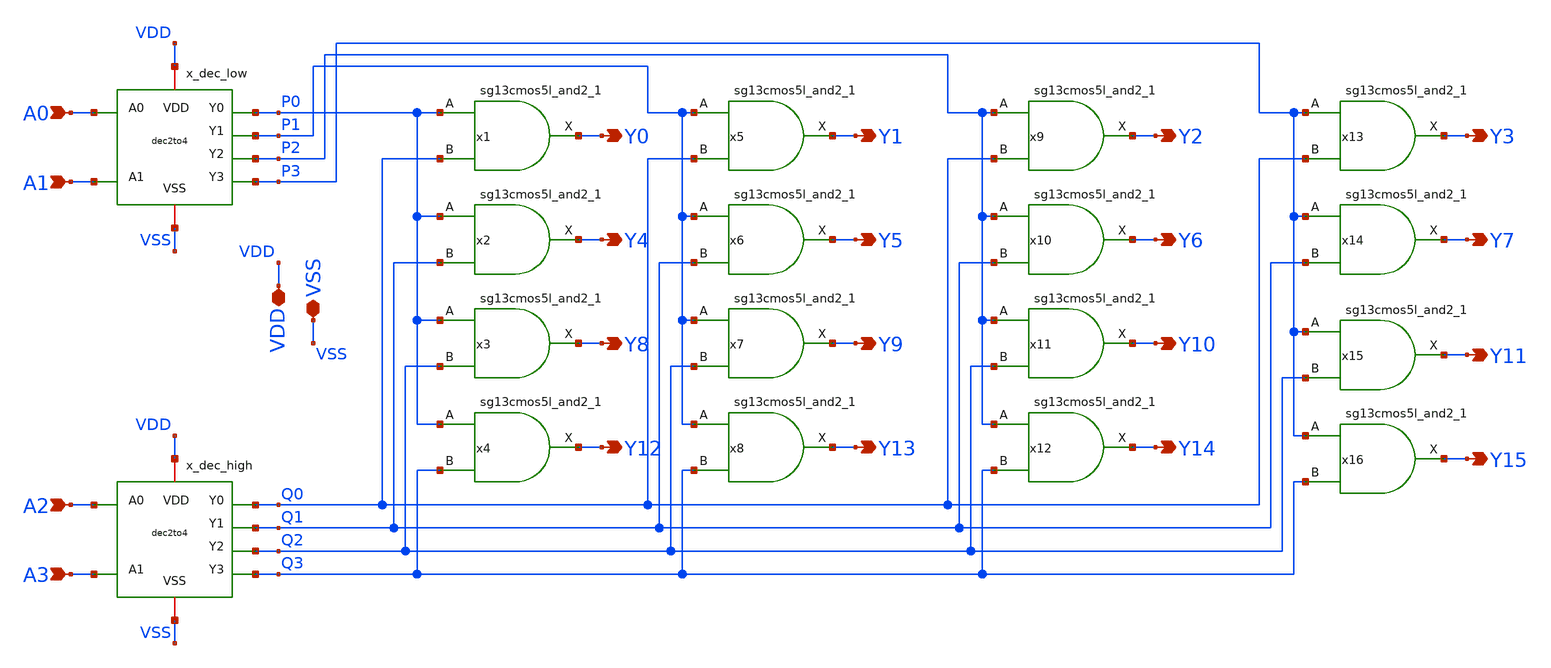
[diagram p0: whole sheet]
** sch_path: designs/libs/core_digital/dec4to16/dec4to16.sch
**.subckt dec4to16 A0 A1 A2 A3 VDD VSS Y0 Y1 Y2 Y3 Y4 Y5 Y6 Y7 Y8 Y9 Y10 Y11 Y12 Y13 Y14 Y15
*.ipin A0
*.ipin A1
*.ipin A2
*.ipin A3
*.iopin VDD
*.iopin VSS
*.opin Y0
*.opin Y1
*.opin Y2
*.opin Y3
*.opin Y4
*.opin Y5
*.opin Y6
*.opin Y7
*.opin Y8
*.opin Y9
*.opin Y10
*.opin Y11
*.opin Y12
*.opin Y13
*.opin Y14
*.opin Y15
x_dec_low A0 A1 P0 P1 P2 P3 VDD VSS dec2to4
x_dec_high A2 A3 Q0 Q1 Q2 Q3 VDD VSS dec2to4
x1 Y0 P0 Q0 VDD VSS sg13cmos5l_and2_1
x2 Y4 P0 Q1 VDD VSS sg13cmos5l_and2_1
x3 Y8 P0 Q2 VDD VSS sg13cmos5l_and2_1
x4 Y12 P0 Q3 VDD VSS sg13cmos5l_and2_1
x5 Y1 P1 Q0 VDD VSS sg13cmos5l_and2_1
x6 Y5 P1 Q1 VDD VSS sg13cmos5l_and2_1
x7 Y9 P1 Q2 VDD VSS sg13cmos5l_and2_1
x8 Y13 P1 Q3 VDD VSS sg13cmos5l_and2_1
x9 Y2 P2 Q0 VDD VSS sg13cmos5l_and2_1
x10 Y6 P2 Q1 VDD VSS sg13cmos5l_and2_1
x11 Y10 P2 Q2 VDD VSS sg13cmos5l_and2_1
x12 Y14 P2 Q3 VDD VSS sg13cmos5l_and2_1
x13 Y3 P3 Q0 VDD VSS sg13cmos5l_and2_1
x14 Y7 P3 Q1 VDD VSS sg13cmos5l_and2_1
x15 Y11 P3 Q2 VDD VSS sg13cmos5l_and2_1
x16 Y15 P3 Q3 VDD VSS sg13cmos5l_and2_1
**.ends

* expanding   symbol:
*+  /foss/designs/Chipalooza/Programmable-Instrumentation-Amplifier-IP/designs/libs/core_digital/dec2to4/dec2to4.sym # of pins=8
** sym_path: /foss/designs/Chipalooza/Programmable-Instrumentation-Amplifier-IP/designs/libs/core_digital/dec2to4/dec2to4.sym
** sch_path: /foss/designs/Chipalooza/Programmable-Instrumentation-Amplifier-IP/designs/libs/core_digital/dec2to4/dec2to4.sch
.subckt dec2to4 A0 A1 Y0 Y1 Y2 Y3 VDD VSS
*.ipin A0
*.ipin A1
*.opin Y0
*.opin Y1
*.opin Y2
*.opin Y3
*.iopin VDD
*.iopin VSS
x1 net2 A0 VDD VSS sg13cmos5l_inv_1
x2 net1 A1 VDD VSS sg13cmos5l_inv_1
x11 Y0 net2 net1 VDD VSS sg13cmos5l_and2_1
x3 Y1 A0 net1 VDD VSS sg13cmos5l_and2_1
x4 Y2 A1 net2 VDD VSS sg13cmos5l_and2_1
x5 Y3 A1 A0 VDD VSS sg13cmos5l_and2_1
.ends

.end
